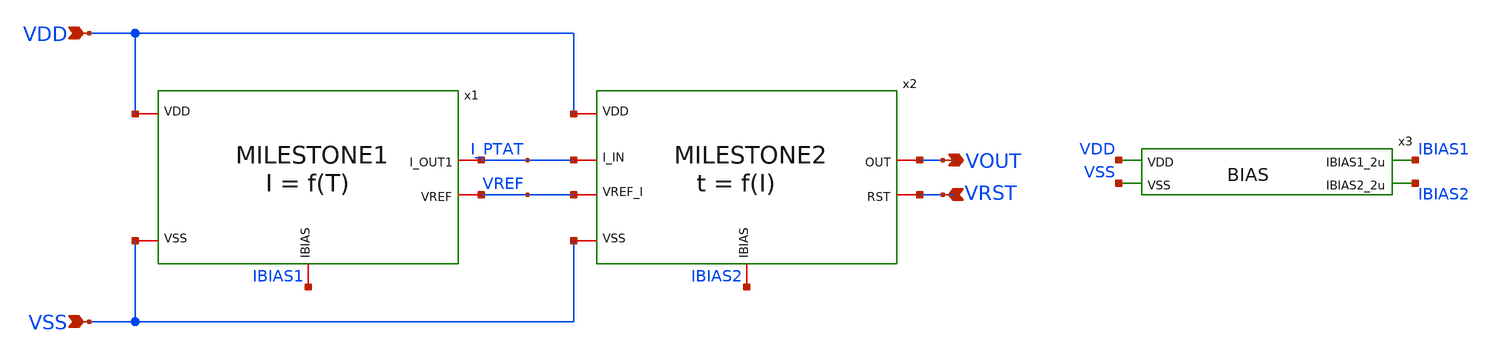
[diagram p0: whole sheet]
** sch_path: design/CNR_GR03_SKY130NM/TOPLEVEL.sch
**.subckt TOPLEVEL VDD VSS VRST VOUT
*.ipin VDD
*.ipin VSS
*.ipin VRST
*.opin VOUT
x1 VDD I_PTAT VREF VSS IBIAS1 MILESTONE1
x2 I_PTAT VREF VOUT VDD VRST VSS IBIAS2 MILESTONE2
x3 VDD IBIAS1 IBIAS2 VSS BIAS
**.ends
.end
